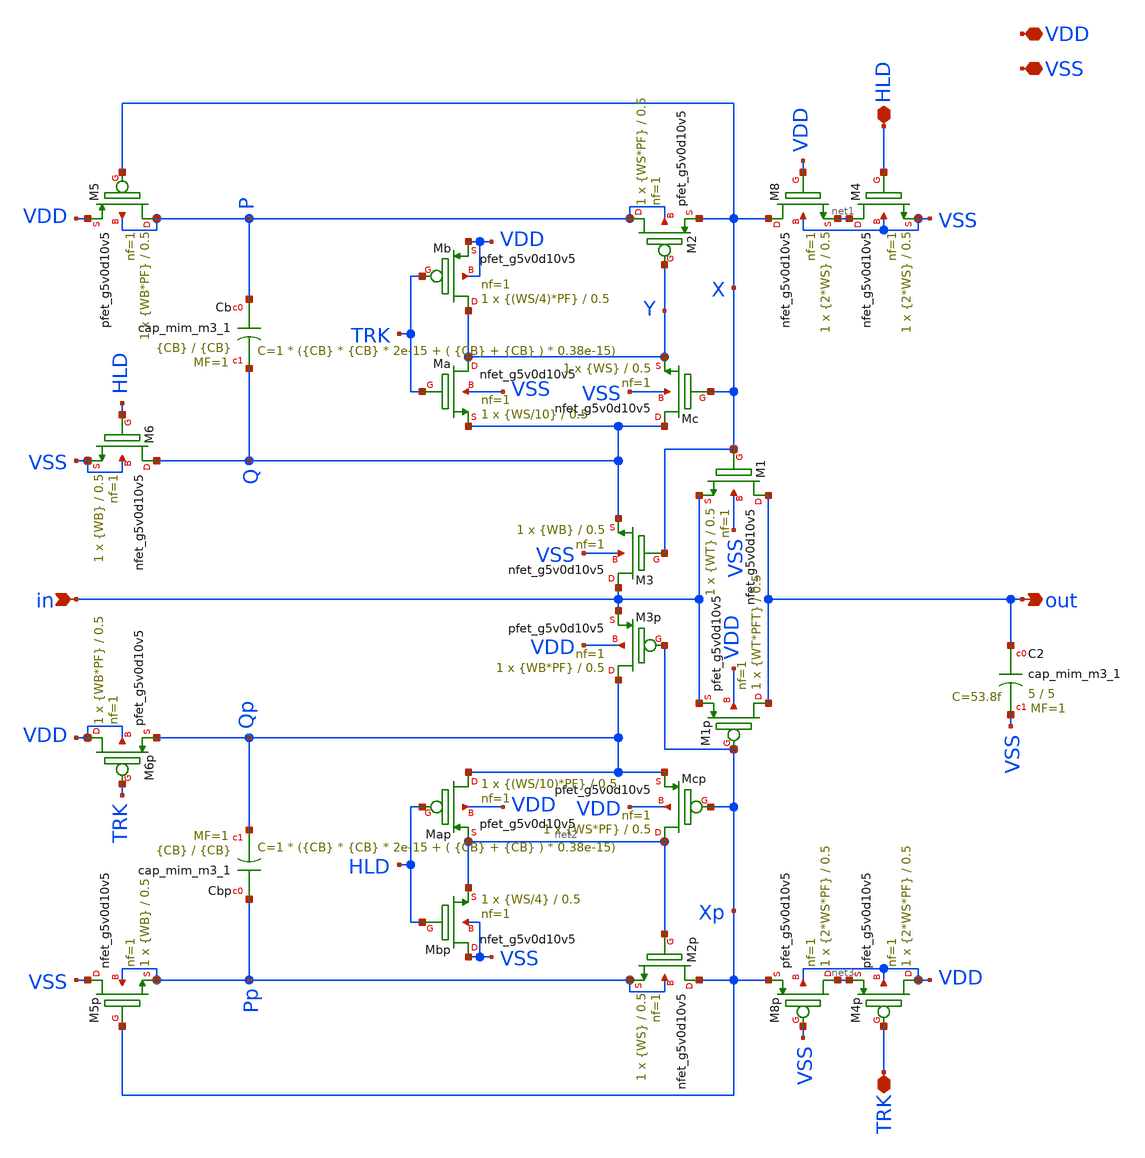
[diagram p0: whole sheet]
** sch_path: xschem/parametric_track_and_hold.sch
**.subckt parametric_track_and_hold VSS VDD in out HLD TRK
*.iopin VSS
*.iopin VDD
*.ipin in
*.opin out
*.iopin HLD
*.iopin TRK
XC2 out VSS sky130_fd_pr__cap_mim_m3_1 W=5 L=5 MF=1 m=1
XM1 out X in VSS sky130_fd_pr__nfet_g5v0d10v5 L=0.5 W={WT} nf=1 ad='int((nf+1)/2) * W/nf * 0.29' as='int((nf+2)/2) * W/nf * 0.29'
+ pd='2*int((nf+1)/2) * (W/nf + 0.29)' ps='2*int((nf+2)/2) * (W/nf + 0.29)' nrd='0.29 / W' nrs='0.29 / W'
+ sa=0 sb=0 sd=0 mult=1 m=1
XM1p out Xp in VDD sky130_fd_pr__pfet_g5v0d10v5 L=0.5 W={WT*PFT} nf=1 ad='int((nf+1)/2) * W/nf * 0.29'
+ as='int((nf+2)/2) * W/nf * 0.29' pd='2*int((nf+1)/2) * (W/nf + 0.29)' ps='2*int((nf+2)/2) * (W/nf + 0.29)'
+ nrd='0.29 / W' nrs='0.29 / W' sa=0 sb=0 sd=0 mult=1 m=1
XM4 net1 HLD VSS VSS sky130_fd_pr__nfet_g5v0d10v5 L=0.5 W={2*WS} nf=1 ad='int((nf+1)/2) * W/nf * 0.29'
+ as='int((nf+2)/2) * W/nf * 0.29' pd='2*int((nf+1)/2) * (W/nf + 0.29)' ps='2*int((nf+2)/2) * (W/nf + 0.29)'
+ nrd='0.29 / W' nrs='0.29 / W' sa=0 sb=0 sd=0 mult=1 m=1
XM2 P Y X P sky130_fd_pr__pfet_g5v0d10v5 L=0.5 W={WS*PF} nf=1 ad='int((nf+1)/2) * W/nf * 0.29' as='int((nf+2)/2) * W/nf * 0.29'
+ pd='2*int((nf+1)/2) * (W/nf + 0.29)' ps='2*int((nf+2)/2) * (W/nf + 0.29)' nrd='0.29 / W' nrs='0.29 / W'
+ sa=0 sb=0 sd=0 mult=1 m=1
XM3 in X Q VSS sky130_fd_pr__nfet_g5v0d10v5 L=0.5 W={WB} nf=1 ad='int((nf+1)/2) * W/nf * 0.29' as='int((nf+2)/2) * W/nf * 0.29'
+ pd='2*int((nf+1)/2) * (W/nf + 0.29)' ps='2*int((nf+2)/2) * (W/nf + 0.29)' nrd='0.29 / W' nrs='0.29 / W'
+ sa=0 sb=0 sd=0 mult=1 m=1
XM6 Q HLD VSS VSS sky130_fd_pr__nfet_g5v0d10v5 L=0.5 W={WB} nf=1 ad='int((nf+1)/2) * W/nf * 0.29' as='int((nf+2)/2) * W/nf * 0.29'
+ pd='2*int((nf+1)/2) * (W/nf + 0.29)' ps='2*int((nf+2)/2) * (W/nf + 0.29)' nrd='0.29 / W' nrs='0.29 / W'
+ sa=0 sb=0 sd=0 mult=1 m=1
XM3p Qp Xp in VDD sky130_fd_pr__pfet_g5v0d10v5 L=0.5 W={WB*PF} nf=1 ad='int((nf+1)/2) * W/nf * 0.29'
+ as='int((nf+2)/2) * W/nf * 0.29' pd='2*int((nf+1)/2) * (W/nf + 0.29)' ps='2*int((nf+2)/2) * (W/nf + 0.29)'
+ nrd='0.29 / W' nrs='0.29 / W' sa=0 sb=0 sd=0 mult=1 m=1
XM5 P X VDD P sky130_fd_pr__pfet_g5v0d10v5 L=0.5 W={WB*PF} nf=1 ad='int((nf+1)/2) * W/nf * 0.29' as='int((nf+2)/2) * W/nf * 0.29'
+ pd='2*int((nf+1)/2) * (W/nf + 0.29)' ps='2*int((nf+2)/2) * (W/nf + 0.29)' nrd='0.29 / W' nrs='0.29 / W'
+ sa=0 sb=0 sd=0 mult=1 m=1
XCb P Q sky130_fd_pr__cap_mim_m3_1 W={CB} L={CB} MF=1 m=1
XM8 X VDD net1 VSS sky130_fd_pr__nfet_g5v0d10v5 L=0.5 W={2*WS} nf=1 ad='int((nf+1)/2) * W/nf * 0.29'
+ as='int((nf+2)/2) * W/nf * 0.29' pd='2*int((nf+1)/2) * (W/nf + 0.29)' ps='2*int((nf+2)/2) * (W/nf + 0.29)'
+ nrd='0.29 / W' nrs='0.29 / W' sa=0 sb=0 sd=0 mult=1 m=1
XMb Y TRK VDD VDD sky130_fd_pr__pfet_g5v0d10v5 L=0.5 W={(WS/4)*PF} nf=1 ad='int((nf+1)/2) * W/nf * 0.29'
+ as='int((nf+2)/2) * W/nf * 0.29' pd='2*int((nf+1)/2) * (W/nf + 0.29)' ps='2*int((nf+2)/2) * (W/nf + 0.29)'
+ nrd='0.29 / W' nrs='0.29 / W' sa=0 sb=0 sd=0 mult=1 m=1
XMa Y TRK Q VSS sky130_fd_pr__nfet_g5v0d10v5 L=0.5 W={WS/10} nf=1 ad='int((nf+1)/2) * W/nf * 0.29' as='int((nf+2)/2) * W/nf * 0.29'
+ pd='2*int((nf+1)/2) * (W/nf + 0.29)' ps='2*int((nf+2)/2) * (W/nf + 0.29)' nrd='0.29 / W' nrs='0.29 / W'
+ sa=0 sb=0 sd=0 mult=1 m=1
XMc Q X Y VSS sky130_fd_pr__nfet_g5v0d10v5 L=0.5 W={WS} nf=1 ad='int((nf+1)/2) * W/nf * 0.29' as='int((nf+2)/2) * W/nf * 0.29'
+ pd='2*int((nf+1)/2) * (W/nf + 0.29)' ps='2*int((nf+2)/2) * (W/nf + 0.29)' nrd='0.29 / W' nrs='0.29 / W'
+ sa=0 sb=0 sd=0 mult=1 m=1
XCbp Pp Qp sky130_fd_pr__cap_mim_m3_1 W={CB} L={CB} MF=1 m=1
XM6p VDD TRK Qp VDD sky130_fd_pr__pfet_g5v0d10v5 L=0.5 W={WB*PF} nf=1 ad='int((nf+1)/2) * W/nf * 0.29'
+ as='int((nf+2)/2) * W/nf * 0.29' pd='2*int((nf+1)/2) * (W/nf + 0.29)' ps='2*int((nf+2)/2) * (W/nf + 0.29)'
+ nrd='0.29 / W' nrs='0.29 / W' sa=0 sb=0 sd=0 mult=1 m=1
XM5p VSS Xp Pp Pp sky130_fd_pr__nfet_g5v0d10v5 L=0.5 W={WB} nf=1 ad='int((nf+1)/2) * W/nf * 0.29' as='int((nf+2)/2) * W/nf * 0.29'
+ pd='2*int((nf+1)/2) * (W/nf + 0.29)' ps='2*int((nf+2)/2) * (W/nf + 0.29)' nrd='0.29 / W' nrs='0.29 / W'
+ sa=0 sb=0 sd=0 mult=1 m=1
XM2p Xp net2 Pp Pp sky130_fd_pr__nfet_g5v0d10v5 L=0.5 W={WS} nf=1 ad='int((nf+1)/2) * W/nf * 0.29' as='int((nf+2)/2) * W/nf * 0.29'
+ pd='2*int((nf+1)/2) * (W/nf + 0.29)' ps='2*int((nf+2)/2) * (W/nf + 0.29)' nrd='0.29 / W' nrs='0.29 / W'
+ sa=0 sb=0 sd=0 mult=1 m=1
XMcp net2 Xp Qp VDD sky130_fd_pr__pfet_g5v0d10v5 L=0.5 W={WS*PF} nf=1 ad='int((nf+1)/2) * W/nf * 0.29'
+ as='int((nf+2)/2) * W/nf * 0.29' pd='2*int((nf+1)/2) * (W/nf + 0.29)' ps='2*int((nf+2)/2) * (W/nf + 0.29)'
+ nrd='0.29 / W' nrs='0.29 / W' sa=0 sb=0 sd=0 mult=1 m=1
XMap Qp HLD net2 VDD sky130_fd_pr__pfet_g5v0d10v5 L=0.5 W={(WS/10)*PF} nf=1 ad='int((nf+1)/2) * W/nf * 0.29'
+ as='int((nf+2)/2) * W/nf * 0.29' pd='2*int((nf+1)/2) * (W/nf + 0.29)' ps='2*int((nf+2)/2) * (W/nf + 0.29)'
+ nrd='0.29 / W' nrs='0.29 / W' sa=0 sb=0 sd=0 mult=1 m=1
XMbp VSS HLD net2 VSS sky130_fd_pr__nfet_g5v0d10v5 L=0.5 W={WS/4} nf=1 ad='int((nf+1)/2) * W/nf * 0.29'
+ as='int((nf+2)/2) * W/nf * 0.29' pd='2*int((nf+1)/2) * (W/nf + 0.29)' ps='2*int((nf+2)/2) * (W/nf + 0.29)'
+ nrd='0.29 / W' nrs='0.29 / W' sa=0 sb=0 sd=0 mult=1 m=1
XM8p net3 VSS Xp VDD sky130_fd_pr__pfet_g5v0d10v5 L=0.5 W={2*WS*PF} nf=1 ad='int((nf+1)/2) * W/nf * 0.29'
+ as='int((nf+2)/2) * W/nf * 0.29' pd='2*int((nf+1)/2) * (W/nf + 0.29)' ps='2*int((nf+2)/2) * (W/nf + 0.29)'
+ nrd='0.29 / W' nrs='0.29 / W' sa=0 sb=0 sd=0 mult=1 m=1
XM4p VDD TRK net3 VDD sky130_fd_pr__pfet_g5v0d10v5 L=0.5 W={2*WS*PF} nf=1 ad='int((nf+1)/2) * W/nf * 0.29'
+ as='int((nf+2)/2) * W/nf * 0.29' pd='2*int((nf+1)/2) * (W/nf + 0.29)' ps='2*int((nf+2)/2) * (W/nf + 0.29)'
+ nrd='0.29 / W' nrs='0.29 / W' sa=0 sb=0 sd=0 mult=1 m=1
**.ends
.end
